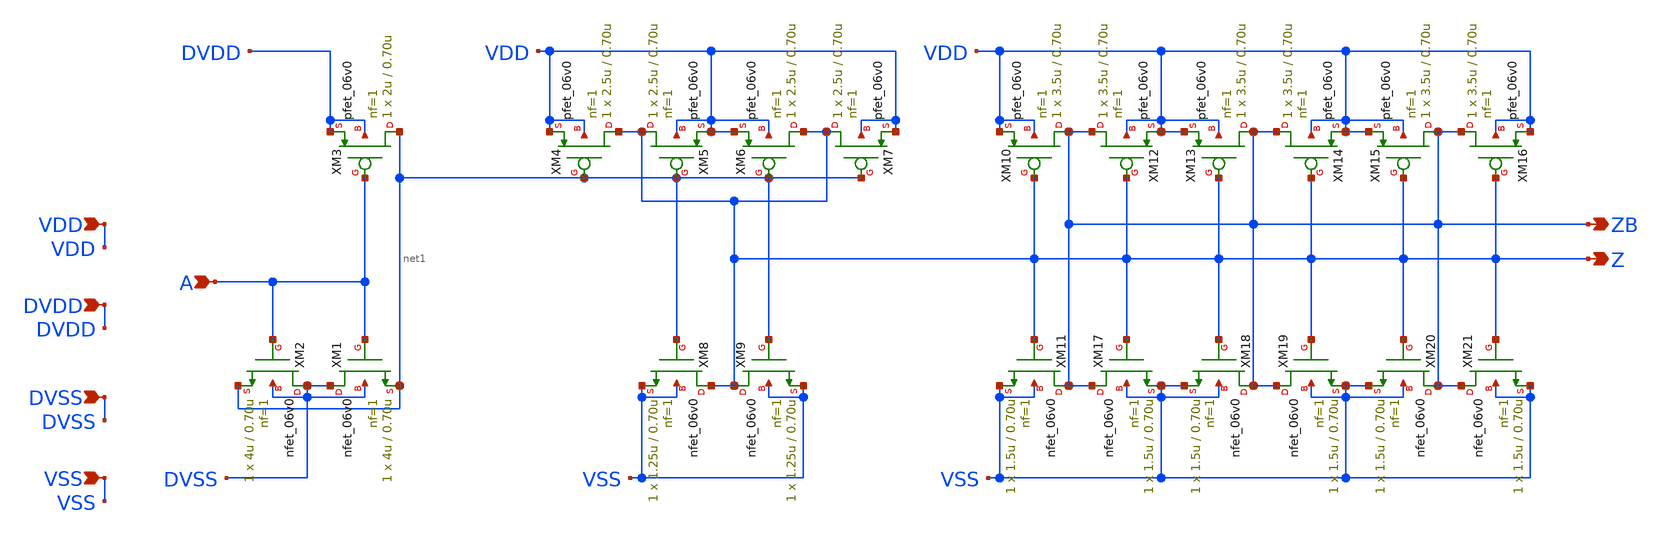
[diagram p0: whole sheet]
** sch_path: gf180mcu_fd_io__bi_24t/comp018green_in_drv.sch
**.subckt comp018green_in_drv A DVDD DVSS Z ZB VDD VSS
*.ipin A
*.ipin DVDD
*.ipin DVSS
*.opin Z
*.opin ZB
*.ipin VDD
*.ipin VSS
XM1 DVSS A net1 DVSS nfet_06v0 L=0.70u W=4u nf=1 ad='int((nf+1)/2) * W/nf * 0.18u' as='int((nf+2)/2) * W/nf * 0.18u'
+ pd='2*int((nf+1)/2) * (W/nf + 0.18u)' ps='2*int((nf+2)/2) * (W/nf + 0.18u)' nrd='0.18u / W' nrs='0.18u / W'
+ sa=0 sb=0 sd=0 m=1
XM3 net1 A DVDD DVDD pfet_06v0 L=0.70u W=2u nf=1 ad='int((nf+1)/2) * W/nf * 0.18u' as='int((nf+2)/2) * W/nf * 0.18u'
+ pd='2*int((nf+1)/2) * (W/nf + 0.18u)' ps='2*int((nf+2)/2) * (W/nf + 0.18u)' nrd='0.18u / W' nrs='0.18u / W'
+ sa=0 sb=0 sd=0 m=1
XM2 DVSS A net1 DVSS nfet_06v0 L=0.70u W=4u nf=1 ad='int((nf+1)/2) * W/nf * 0.18u' as='int((nf+2)/2) * W/nf * 0.18u'
+ pd='2*int((nf+1)/2) * (W/nf + 0.18u)' ps='2*int((nf+2)/2) * (W/nf + 0.18u)' nrd='0.18u / W' nrs='0.18u / W'
+ sa=0 sb=0 sd=0 m=1
XM4 Z net1 VDD VDD pfet_06v0 L=0.70u W=2.5u nf=1 ad='int((nf+1)/2) * W/nf * 0.18u' as='int((nf+2)/2) * W/nf * 0.18u'
+ pd='2*int((nf+1)/2) * (W/nf + 0.18u)' ps='2*int((nf+2)/2) * (W/nf + 0.18u)' nrd='0.18u / W' nrs='0.18u / W'
+ sa=0 sb=0 sd=0 m=1
XM5 Z net1 VDD VDD pfet_06v0 L=0.70u W=2.5u nf=1 ad='int((nf+1)/2) * W/nf * 0.18u' as='int((nf+2)/2) * W/nf * 0.18u'
+ pd='2*int((nf+1)/2) * (W/nf + 0.18u)' ps='2*int((nf+2)/2) * (W/nf + 0.18u)' nrd='0.18u / W' nrs='0.18u / W'
+ sa=0 sb=0 sd=0 m=1
XM6 Z net1 VDD VDD pfet_06v0 L=0.70u W=2.5u nf=1 ad='int((nf+1)/2) * W/nf * 0.18u' as='int((nf+2)/2) * W/nf * 0.18u'
+ pd='2*int((nf+1)/2) * (W/nf + 0.18u)' ps='2*int((nf+2)/2) * (W/nf + 0.18u)' nrd='0.18u / W' nrs='0.18u / W'
+ sa=0 sb=0 sd=0 m=1
XM7 Z net1 VDD VDD pfet_06v0 L=0.70u W=2.5u nf=1 ad='int((nf+1)/2) * W/nf * 0.18u' as='int((nf+2)/2) * W/nf * 0.18u'
+ pd='2*int((nf+1)/2) * (W/nf + 0.18u)' ps='2*int((nf+2)/2) * (W/nf + 0.18u)' nrd='0.18u / W' nrs='0.18u / W'
+ sa=0 sb=0 sd=0 m=1
XM8 Z net1 VSS VSS nfet_06v0 L=0.70u W=1.25u nf=1 ad='int((nf+1)/2) * W/nf * 0.18u' as='int((nf+2)/2) * W/nf * 0.18u'
+ pd='2*int((nf+1)/2) * (W/nf + 0.18u)' ps='2*int((nf+2)/2) * (W/nf + 0.18u)' nrd='0.18u / W' nrs='0.18u / W'
+ sa=0 sb=0 sd=0 m=1
XM9 Z net1 VSS VSS nfet_06v0 L=0.70u W=1.25u nf=1 ad='int((nf+1)/2) * W/nf * 0.18u' as='int((nf+2)/2) * W/nf * 0.18u'
+ pd='2*int((nf+1)/2) * (W/nf + 0.18u)' ps='2*int((nf+2)/2) * (W/nf + 0.18u)' nrd='0.18u / W' nrs='0.18u / W'
+ sa=0 sb=0 sd=0 m=1
XM10 ZB Z VDD VDD pfet_06v0 L=0.70u W=3.5u nf=1 ad='int((nf+1)/2) * W/nf * 0.18u' as='int((nf+2)/2) * W/nf * 0.18u'
+ pd='2*int((nf+1)/2) * (W/nf + 0.18u)' ps='2*int((nf+2)/2) * (W/nf + 0.18u)' nrd='0.18u / W' nrs='0.18u / W'
+ sa=0 sb=0 sd=0 m=1
XM11 ZB Z VSS VSS nfet_06v0 L=0.70u W=1.5u nf=1 ad='int((nf+1)/2) * W/nf * 0.18u' as='int((nf+2)/2) * W/nf * 0.18u'
+ pd='2*int((nf+1)/2) * (W/nf + 0.18u)' ps='2*int((nf+2)/2) * (W/nf + 0.18u)' nrd='0.18u / W' nrs='0.18u / W'
+ sa=0 sb=0 sd=0 m=1
XM12 ZB Z VDD VDD pfet_06v0 L=0.70u W=3.5u nf=1 ad='int((nf+1)/2) * W/nf * 0.18u' as='int((nf+2)/2) * W/nf * 0.18u'
+ pd='2*int((nf+1)/2) * (W/nf + 0.18u)' ps='2*int((nf+2)/2) * (W/nf + 0.18u)' nrd='0.18u / W' nrs='0.18u / W'
+ sa=0 sb=0 sd=0 m=1
XM13 ZB Z VDD VDD pfet_06v0 L=0.70u W=3.5u nf=1 ad='int((nf+1)/2) * W/nf * 0.18u' as='int((nf+2)/2) * W/nf * 0.18u'
+ pd='2*int((nf+1)/2) * (W/nf + 0.18u)' ps='2*int((nf+2)/2) * (W/nf + 0.18u)' nrd='0.18u / W' nrs='0.18u / W'
+ sa=0 sb=0 sd=0 m=1
XM14 ZB Z VDD VDD pfet_06v0 L=0.70u W=3.5u nf=1 ad='int((nf+1)/2) * W/nf * 0.18u' as='int((nf+2)/2) * W/nf * 0.18u'
+ pd='2*int((nf+1)/2) * (W/nf + 0.18u)' ps='2*int((nf+2)/2) * (W/nf + 0.18u)' nrd='0.18u / W' nrs='0.18u / W'
+ sa=0 sb=0 sd=0 m=1
XM15 ZB Z VDD VDD pfet_06v0 L=0.70u W=3.5u nf=1 ad='int((nf+1)/2) * W/nf * 0.18u' as='int((nf+2)/2) * W/nf * 0.18u'
+ pd='2*int((nf+1)/2) * (W/nf + 0.18u)' ps='2*int((nf+2)/2) * (W/nf + 0.18u)' nrd='0.18u / W' nrs='0.18u / W'
+ sa=0 sb=0 sd=0 m=1
XM16 ZB Z VDD VDD pfet_06v0 L=0.70u W=3.5u nf=1 ad='int((nf+1)/2) * W/nf * 0.18u' as='int((nf+2)/2) * W/nf * 0.18u'
+ pd='2*int((nf+1)/2) * (W/nf + 0.18u)' ps='2*int((nf+2)/2) * (W/nf + 0.18u)' nrd='0.18u / W' nrs='0.18u / W'
+ sa=0 sb=0 sd=0 m=1
XM17 ZB Z VSS VSS nfet_06v0 L=0.70u W=1.5u nf=1 ad='int((nf+1)/2) * W/nf * 0.18u' as='int((nf+2)/2) * W/nf * 0.18u'
+ pd='2*int((nf+1)/2) * (W/nf + 0.18u)' ps='2*int((nf+2)/2) * (W/nf + 0.18u)' nrd='0.18u / W' nrs='0.18u / W'
+ sa=0 sb=0 sd=0 m=1
XM18 ZB Z VSS VSS nfet_06v0 L=0.70u W=1.5u nf=1 ad='int((nf+1)/2) * W/nf * 0.18u' as='int((nf+2)/2) * W/nf * 0.18u'
+ pd='2*int((nf+1)/2) * (W/nf + 0.18u)' ps='2*int((nf+2)/2) * (W/nf + 0.18u)' nrd='0.18u / W' nrs='0.18u / W'
+ sa=0 sb=0 sd=0 m=1
XM19 ZB Z VSS VSS nfet_06v0 L=0.70u W=1.5u nf=1 ad='int((nf+1)/2) * W/nf * 0.18u' as='int((nf+2)/2) * W/nf * 0.18u'
+ pd='2*int((nf+1)/2) * (W/nf + 0.18u)' ps='2*int((nf+2)/2) * (W/nf + 0.18u)' nrd='0.18u / W' nrs='0.18u / W'
+ sa=0 sb=0 sd=0 m=1
XM20 ZB Z VSS VSS nfet_06v0 L=0.70u W=1.5u nf=1 ad='int((nf+1)/2) * W/nf * 0.18u' as='int((nf+2)/2) * W/nf * 0.18u'
+ pd='2*int((nf+1)/2) * (W/nf + 0.18u)' ps='2*int((nf+2)/2) * (W/nf + 0.18u)' nrd='0.18u / W' nrs='0.18u / W'
+ sa=0 sb=0 sd=0 m=1
XM21 ZB Z VSS VSS nfet_06v0 L=0.70u W=1.5u nf=1 ad='int((nf+1)/2) * W/nf * 0.18u' as='int((nf+2)/2) * W/nf * 0.18u'
+ pd='2*int((nf+1)/2) * (W/nf + 0.18u)' ps='2*int((nf+2)/2) * (W/nf + 0.18u)' nrd='0.18u / W' nrs='0.18u / W'
+ sa=0 sb=0 sd=0 m=1
**.ends
.end
